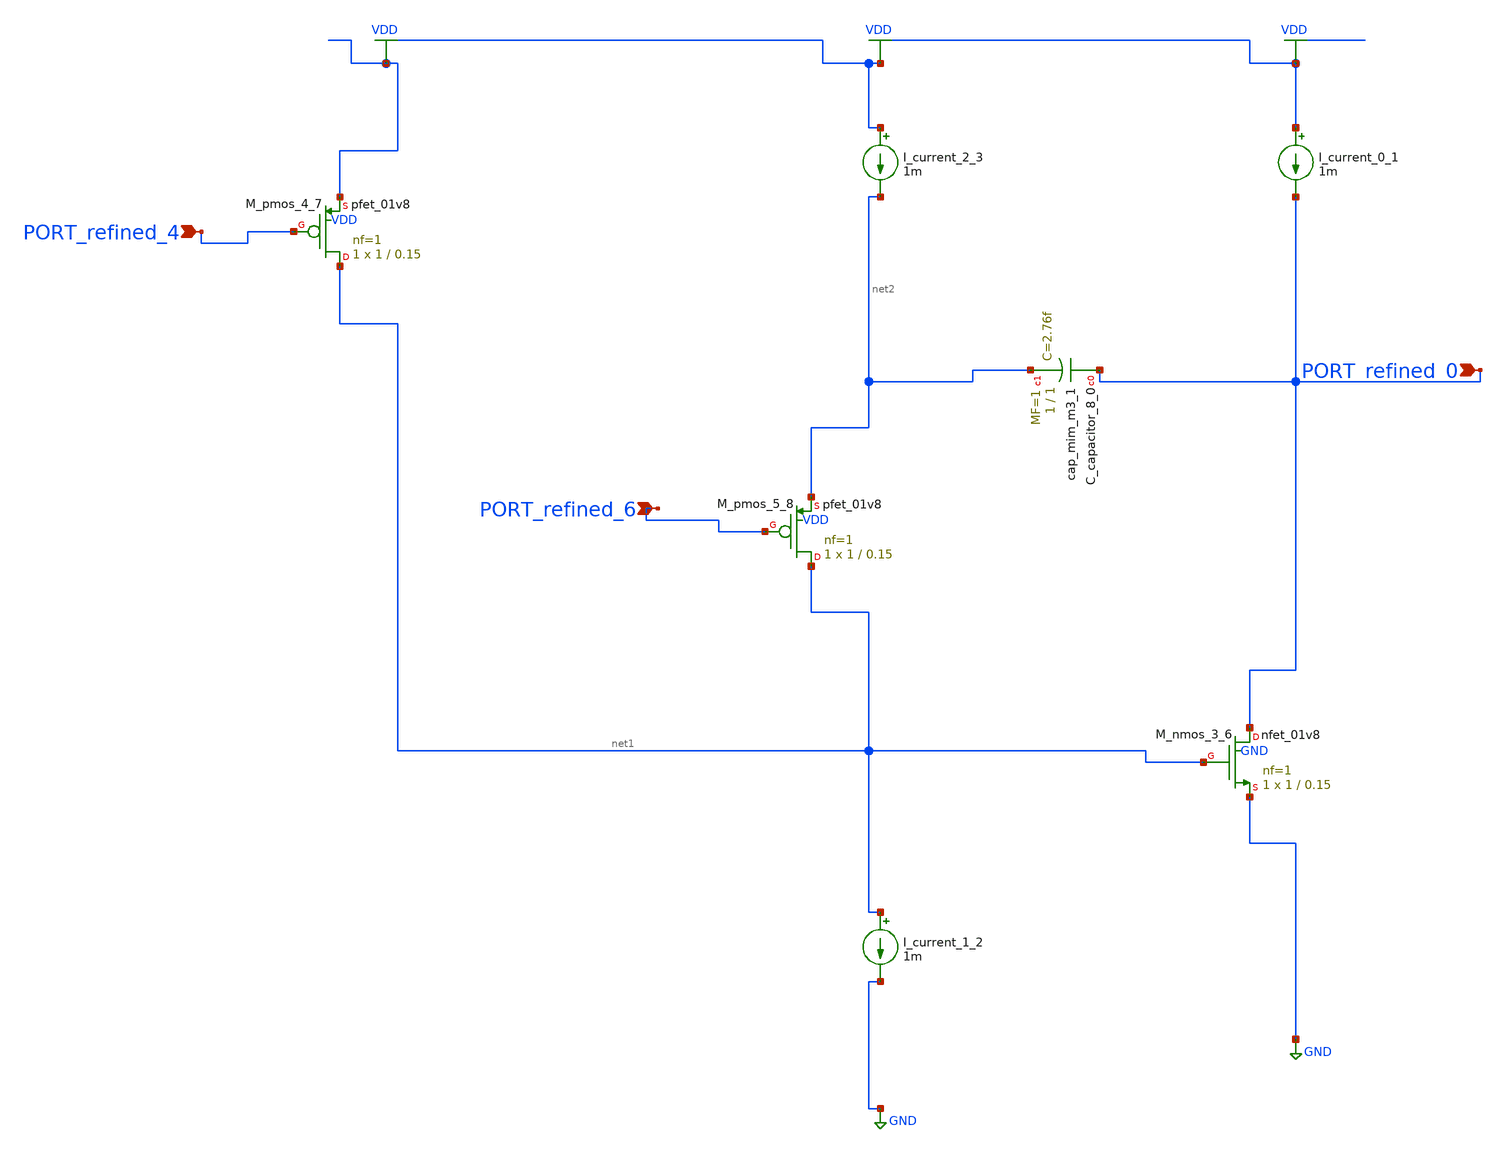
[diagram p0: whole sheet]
** sch_path: schematics/AMSNet/737.sch
**.subckt 737 PORT_refined_0 PORT_refined_4 PORT_refined_6
*.ipin PORT_refined_0
*.ipin PORT_refined_4
*.ipin PORT_refined_6
XC_capacitor_8_0 PORT_refined_0 net2 sky130_fd_pr__cap_mim_m3_1 W=1 L=1 MF=1 m=1
I_current_0_1 VDD PORT_refined_0 1m
I_current_1_2 net1 GND 1m
I_current_2_3 VDD net2 1m
XM_nmos_3_6 PORT_refined_0 net1 GND GND sky130_fd_pr__nfet_01v8 L=0.15 W=1 nf=1 ad='int((1 + 1)/2) * 1 / 1 * 0.29'
+ as='int((1 + 2)/2) * 1 / 1 * 0.29' pd='2*int((1 + 1)/2) * (1 / 1 + 0.29)' ps='2*int((1 + 2)/2) * (1 / 1 + 0.29)'
+ nrd='0.29 / 1 ' nrs='0.29 / 1 ' sa=0 sb=0 sd=0 mult=1 m=1
XM_pmos_4_7 net1 PORT_refined_4 VDD VDD sky130_fd_pr__pfet_01v8 L=0.15 W=1 nf=1 ad='int((1 + 1)/2) * 1 / 1 * 0.29'
+ as='int((1 + 2)/2) * 1 / 1 * 0.29' pd='2*int((1 + 1)/2) * (1 / 1 + 0.29)' ps='2*int((1 + 2)/2) * (1 / 1 + 0.29)'
+ nrd='0.29 / 1 ' nrs='0.29 / 1 ' sa=0 sb=0 sd=0 mult=1 m=1
XM_pmos_5_8 net1 PORT_refined_6 net2 VDD sky130_fd_pr__pfet_01v8 L=0.15 W=1 nf=1 ad='int((1 + 1)/2) * 1 / 1 * 0.29'
+ as='int((1 + 2)/2) * 1 / 1 * 0.29' pd='2*int((1 + 1)/2) * (1 / 1 + 0.29)' ps='2*int((1 + 2)/2) * (1 / 1 + 0.29)'
+ nrd='0.29 / 1 ' nrs='0.29 / 1 ' sa=0 sb=0 sd=0 mult=1 m=1
**.ends
.GLOBAL GND
.GLOBAL VDD
.end
